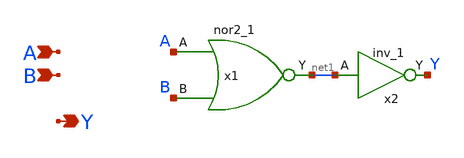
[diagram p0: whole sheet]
** sch_path: designs/libs/core_fpga/OR2_1/OR2_1.sch
**.subckt OR2_1 A B Y
*.ipin A
*.ipin B
*.opin Y
x1 A B VSSd VDDd VSSd VDDd net1 gf180mcu_fd_sc_mcu9t5v0__nor2_1
x2 net1 VSSd VDDd VSSd VDDd Y gf180mcu_fd_sc_mcu9t5v0__inv_1
**.ends
.end
